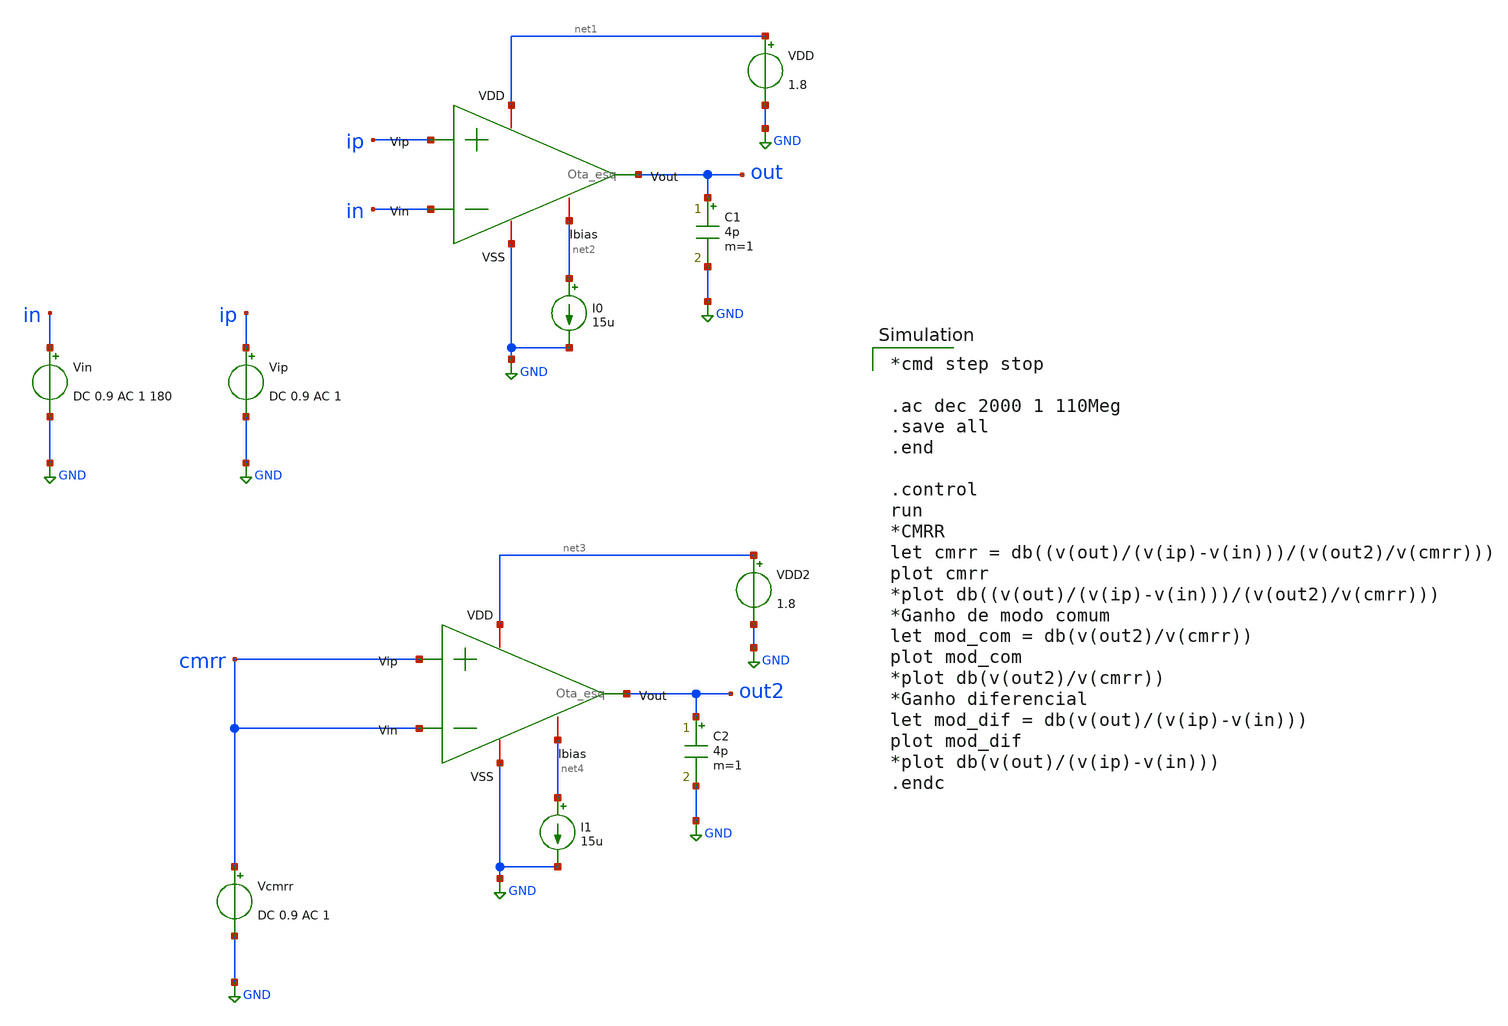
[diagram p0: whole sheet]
** sch_path: xschem/Ota_cmrr_tb.sch
**.subckt Ota_cmrr_tb
x1 net1 in ip out net2 GND Ota_esq
Vip ip GND DC 0.9 AC 1
VDD net1 GND 1.8
I0 net2 GND 15u
x2 net3 cmrr cmrr out2 net4 GND Ota_esq
Vcmrr cmrr GND DC 0.9 AC 1
VDD2 net3 GND 1.8
I1 net4 GND 15u
Vin in GND DC 0.9 AC 1 180
C1 out GND 4p m=1
C2 out2 GND 4p m=1
**** begin user architecture code

** opencircuitdesign pdks install
.lib $::SKYWATER_MODELS/sky130.lib.spice tt



*cmd step stop

.ac dec 2000 1 110Meg
.save all
.end

.control
run
*CMRR
let cmrr = db((v(out)/(v(ip)-v(in)))/(v(out2)/v(cmrr)))
plot cmrr
*plot db((v(out)/(v(ip)-v(in)))/(v(out2)/v(cmrr)))
*Ganho de modo comum
let mod_com = db(v(out2)/v(cmrr))
plot mod_com
*plot db(v(out2)/v(cmrr))
*Ganho diferencial
let mod_dif = db(v(out)/(v(ip)-v(in)))
plot mod_dif
*plot db(v(out)/(v(ip)-v(in)))
.endc

**** end user architecture code
**.ends

* expanding   symbol:  Ota_esq.sym # of pins=6
** sym_path: Ota_esq.sym
** sch_path: Ota_esq.sch
.subckt Ota_esq VDD Vin Vip Vout Ibias VSS
*.ipin Vin
*.ipin Vip
*.iopin VDD
*.iopin VSS
*.iopin Ibias
*.opin Vout
XM1 net1 Vin net3 net3 sky130_fd_pr__pfet_01v8 L=0.25 W=2.899 nf=1 ad='int((nf+1)/2) * W/nf * 0.29' as='int((nf+2)/2) * W/nf * 0.29'
+ pd='2*int((nf+1)/2) * (W/nf + 0.29)' ps='2*int((nf+2)/2) * (W/nf + 0.29)' nrd='0.29 / W' nrs='0.29 / W'
+ sa=0 sb=0 sd=0 mult=1 m=1
XM2 net2 Vip net3 net3 sky130_fd_pr__pfet_01v8 L=0.25 W=2.899 nf=1 ad='int((nf+1)/2) * W/nf * 0.29' as='int((nf+2)/2) * W/nf * 0.29'
+ pd='2*int((nf+1)/2) * (W/nf + 0.29)' ps='2*int((nf+2)/2) * (W/nf + 0.29)' nrd='0.29 / W' nrs='0.29 / W'
+ sa=0 sb=0 sd=0 mult=1 m=1
XM3 net1 net1 VSS VSS sky130_fd_pr__nfet_01v8 L=0.25 W=0.667 nf=1 ad='int((nf+1)/2) * W/nf * 0.29' as='int((nf+2)/2) * W/nf * 0.29'
+ pd='2*int((nf+1)/2) * (W/nf + 0.29)' ps='2*int((nf+2)/2) * (W/nf + 0.29)' nrd='0.29 / W' nrs='0.29 / W'
+ sa=0 sb=0 sd=0 mult=1 m=1
XM4 net2 net1 VSS VSS sky130_fd_pr__nfet_01v8 L=0.25 W=0.667 nf=1 ad='int((nf+1)/2) * W/nf * 0.29' as='int((nf+2)/2) * W/nf * 0.29'
+ pd='2*int((nf+1)/2) * (W/nf + 0.29)' ps='2*int((nf+2)/2) * (W/nf + 0.29)' nrd='0.29 / W' nrs='0.29 / W'
+ sa=0 sb=0 sd=0 mult=1 m=1
XM5 net3 Ibias VDD VDD sky130_fd_pr__pfet_01v8 L=0.25 W=3.333 nf=1 ad='int((nf+1)/2) * W/nf * 0.29' as='int((nf+2)/2) * W/nf * 0.29'
+ pd='2*int((nf+1)/2) * (W/nf + 0.29)' ps='2*int((nf+2)/2) * (W/nf + 0.29)' nrd='0.29 / W' nrs='0.29 / W'
+ sa=0 sb=0 sd=0 mult=1 m=1
XM8 Ibias Ibias VDD VDD sky130_fd_pr__pfet_01v8 L=0.25 W=3.333 nf=1 ad='int((nf+1)/2) * W/nf * 0.29'
+ as='int((nf+2)/2) * W/nf * 0.29' pd='2*int((nf+1)/2) * (W/nf + 0.29)' ps='2*int((nf+2)/2) * (W/nf + 0.29)'
+ nrd='0.29 / W' nrs='0.29 / W' sa=0 sb=0 sd=0 mult=1 m=1
XM6 Vout Ibias VDD VDD sky130_fd_pr__pfet_01v8 L=0.25 W=17.279 nf=1 ad='int((nf+1)/2) * W/nf * 0.29'
+ as='int((nf+2)/2) * W/nf * 0.29' pd='2*int((nf+1)/2) * (W/nf + 0.29)' ps='2*int((nf+2)/2) * (W/nf + 0.29)'
+ nrd='0.29 / W' nrs='0.29 / W' sa=0 sb=0 sd=0 mult=1 m=1
XM7 Vout net2 VSS VSS sky130_fd_pr__nfet_01v8 L=0.25 W=6.192 nf=1 ad='int((nf+1)/2) * W/nf * 0.29' as='int((nf+2)/2) * W/nf * 0.29'
+ pd='2*int((nf+1)/2) * (W/nf + 0.29)' ps='2*int((nf+2)/2) * (W/nf + 0.29)' nrd='0.29 / W' nrs='0.29 / W'
+ sa=0 sb=0 sd=0 mult=1 m=1
XC1 net2 Vout sky130_fd_pr__cap_mim_m3_1 W=23 L=23 MF=1 m=1
.ends

.GLOBAL GND
.end
